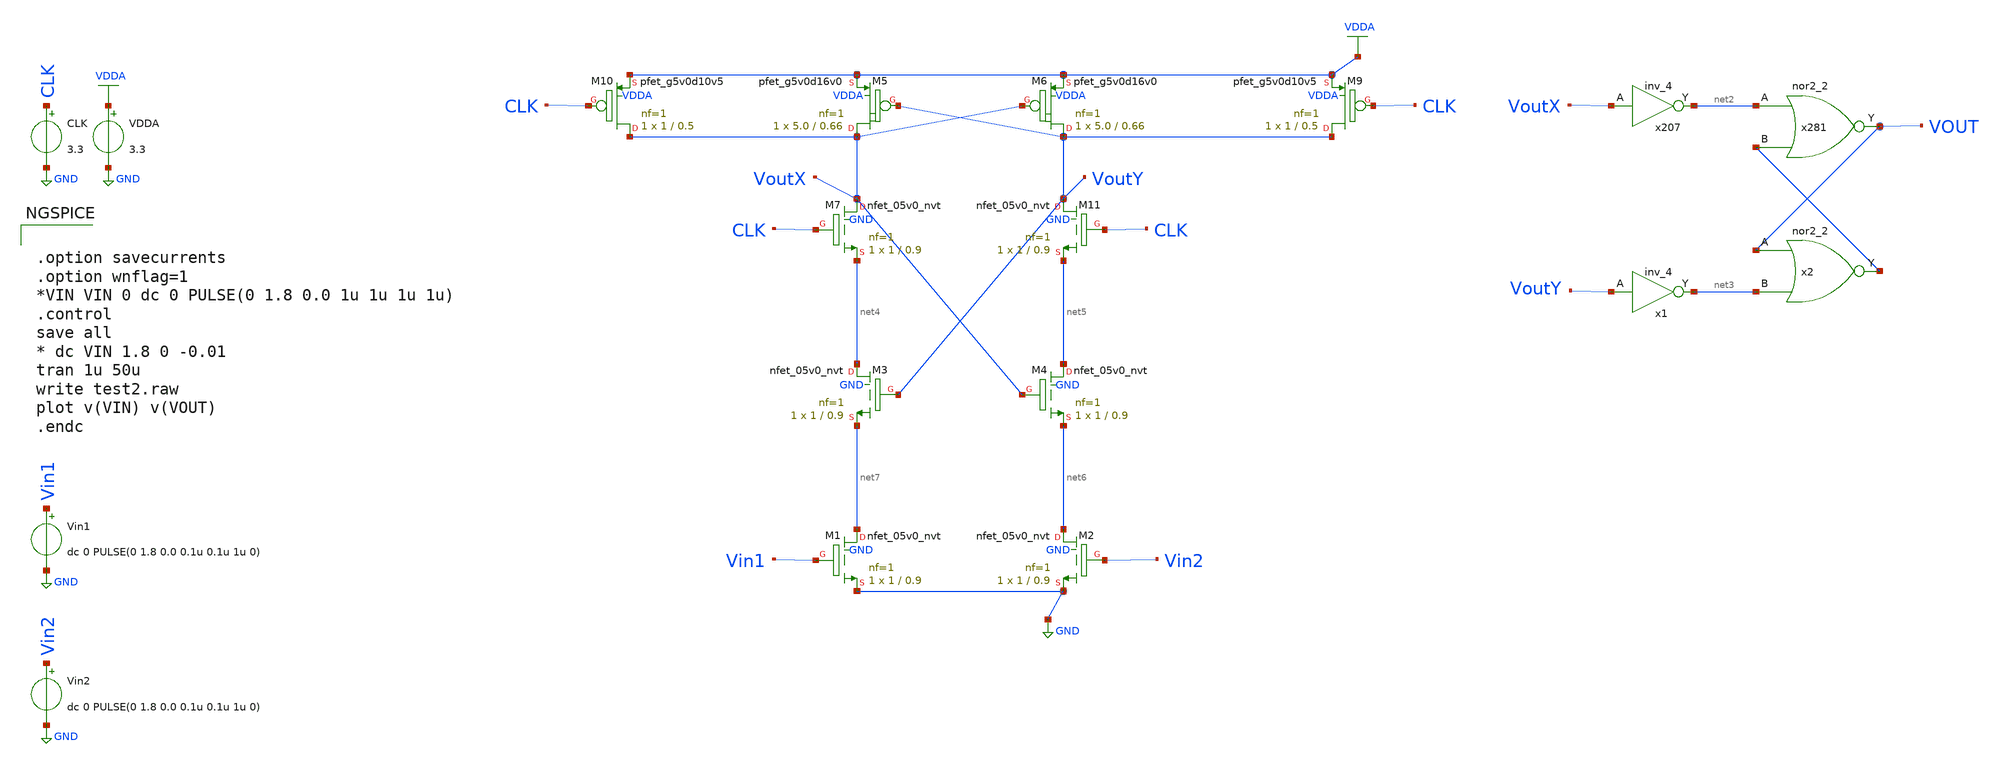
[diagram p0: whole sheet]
** sch_path: xschem/StrongARMLatch.sch
**.subckt StrongARMLatch
VDDA VDDA GND 3.3
XM4 net5 VoutX net6 GND sky130_fd_pr__nfet_05v0_nvt L=0.9 W=1 nf=1 ad='int((1 + 1)/2) * 1 / 1 * 0.29'
+ as='int((1 + 2)/2) * 1 / 1 * 0.29' pd='2*int((1 + 1)/2) * (1 / 1 + 0.29)' ps='2*int((1 + 2)/2) * (1 / 1 + 0.29)'
+ nrd='0.29 / 1 ' nrs='0.29 / 1 ' sa=0 sb=0 sd=0 mult=1 m=1
XM3 net4 VoutY net7 GND sky130_fd_pr__nfet_05v0_nvt L=0.9 W=1 nf=1 ad='int((1 + 1)/2) * 1 / 1 * 0.29'
+ as='int((1 + 2)/2) * 1 / 1 * 0.29' pd='2*int((1 + 1)/2) * (1 / 1 + 0.29)' ps='2*int((1 + 2)/2) * (1 / 1 + 0.29)'
+ nrd='0.29 / 1 ' nrs='0.29 / 1 ' sa=0 sb=0 sd=0 mult=1 m=1
XM6 VoutY VoutX VDDA VDDA sky130_fd_pr__pfet_g5v0d16v0 L=0.66 W=5.0 nf=1 ad='int((1 + 1)/2) * 5.0 / 1 * 0.29'
+ as='int((1 + 2)/2) * 5.0 / 1 * 0.29' pd='2*int((1 + 1)/2) * (5.0 / 1 + 0.29)' ps='2*int((1 + 2)/2) * (5.0 / 1 + 0.29)'
+ nrd='0.29 / 5.0 ' nrs='0.29 / 5.0 ' sa=0 sb=0 sd=0 mult=1 m=1
XM5 VoutX VoutY VDDA VDDA sky130_fd_pr__pfet_g5v0d16v0 L=0.66 W=5.0 nf=1 ad='int((1 + 1)/2) * 5.0 / 1 * 0.29'
+ as='int((1 + 2)/2) * 5.0 / 1 * 0.29' pd='2*int((1 + 1)/2) * (5.0 / 1 + 0.29)' ps='2*int((1 + 2)/2) * (5.0 / 1 + 0.29)'
+ nrd='0.29 / 5.0 ' nrs='0.29 / 5.0 ' sa=0 sb=0 sd=0 mult=1 m=1
XM2 net6 Vin2 GND GND sky130_fd_pr__nfet_05v0_nvt L=0.9 W=1 nf=1 ad='int((1 + 1)/2) * 1 / 1 * 0.29' as='int((1 + 2)/2) * 1 / 1 * 0.29'
+ pd='2*int((1 + 1)/2) * (1 / 1 + 0.29)' ps='2*int((1 + 2)/2) * (1 / 1 + 0.29)' nrd='0.29 / 1 ' nrs='0.29 / 1 '
+ sa=0 sb=0 sd=0 mult=1 m=1
XM10 VoutX CLK VDDA VDDA sky130_fd_pr__pfet_g5v0d10v5 L=0.5 W=1 nf=1 ad='int((nf+1)/2) * W/nf * 0.29'
+ as='int((nf+2)/2) * W/nf * 0.29' pd='2*int((nf+1)/2) * (W/nf + 0.29)' ps='2*int((nf+2)/2) * (W/nf + 0.29)'
+ nrd='0.29 / W' nrs='0.29 / W' sa=0 sb=0 sd=0 mult=1 m=1
XM9 VoutY CLK VDDA VDDA sky130_fd_pr__pfet_g5v0d10v5 L=0.5 W=1 nf=1 ad='int((nf+1)/2) * W/nf * 0.29'
+ as='int((nf+2)/2) * W/nf * 0.29' pd='2*int((nf+1)/2) * (W/nf + 0.29)' ps='2*int((nf+2)/2) * (W/nf + 0.29)'
+ nrd='0.29 / W' nrs='0.29 / W' sa=0 sb=0 sd=0 mult=1 m=1
XM7 VoutX CLK net4 GND sky130_fd_pr__nfet_05v0_nvt L=0.9 W=1 nf=1 ad='int((1 + 1)/2) * 1 / 1 * 0.29'
+ as='int((1 + 2)/2) * 1 / 1 * 0.29' pd='2*int((1 + 1)/2) * (1 / 1 + 0.29)' ps='2*int((1 + 2)/2) * (1 / 1 + 0.29)'
+ nrd='0.29 / 1 ' nrs='0.29 / 1 ' sa=0 sb=0 sd=0 mult=1 m=1
CLK CLK GND 3.3
Vin1 Vin1 GND dc 0 PULSE(0 1.8 0.0 0.1u 0.1u 1u 0)
Vin2 Vin2 GND dc 0 PULSE(0 1.8 0.0 0.1u 0.1u 1u 0)
XM11 VoutY CLK net5 GND sky130_fd_pr__nfet_05v0_nvt L=0.9 W=1 nf=1 ad='int((1 + 1)/2) * 1 / 1 * 0.29'
+ as='int((1 + 2)/2) * 1 / 1 * 0.29' pd='2*int((1 + 1)/2) * (1 / 1 + 0.29)' ps='2*int((1 + 2)/2) * (1 / 1 + 0.29)'
+ nrd='0.29 / 1 ' nrs='0.29 / 1 ' sa=0 sb=0 sd=0 mult=1 m=1
XM1 net7 Vin1 GND GND sky130_fd_pr__nfet_05v0_nvt L=0.9 W=1 nf=1 ad='int((1 + 1)/2) * 1 / 1 * 0.29' as='int((1 + 2)/2) * 1 / 1 * 0.29'
+ pd='2*int((1 + 1)/2) * (1 / 1 + 0.29)' ps='2*int((1 + 2)/2) * (1 / 1 + 0.29)' nrd='0.29 / 1 ' nrs='0.29 / 1 '
+ sa=0 sb=0 sd=0 mult=1 m=1
x207 VoutX GND GND VCC VCC net2 sky130_fd_sc_hd__inv_4
x1 VoutY GND GND VCC VCC net3 sky130_fd_sc_hd__inv_4
x281 net2 net1 GND GND VCC VCC VOUT sky130_fd_sc_hd__nor2_2
x2 VOUT net3 GND GND VCC VCC net1 sky130_fd_sc_hd__nor2_2
**** begin user architecture code

** opencircuitdesign pdks install
.lib $::SKYWATER_MODELS/sky130.lib.spice tt




.option savecurrents
.option wnflag=1
*VIN VIN 0 dc 0 PULSE(0 1.8 0.0 1u 1u 1u 1u)
.control
save all
* dc VIN 1.8 0 -0.01
tran 1u 50u
write test2.raw
plot v(VIN) v(VOUT)
.endc


**** end user architecture code
**.ends
.GLOBAL GND
.GLOBAL VDDA
.end
